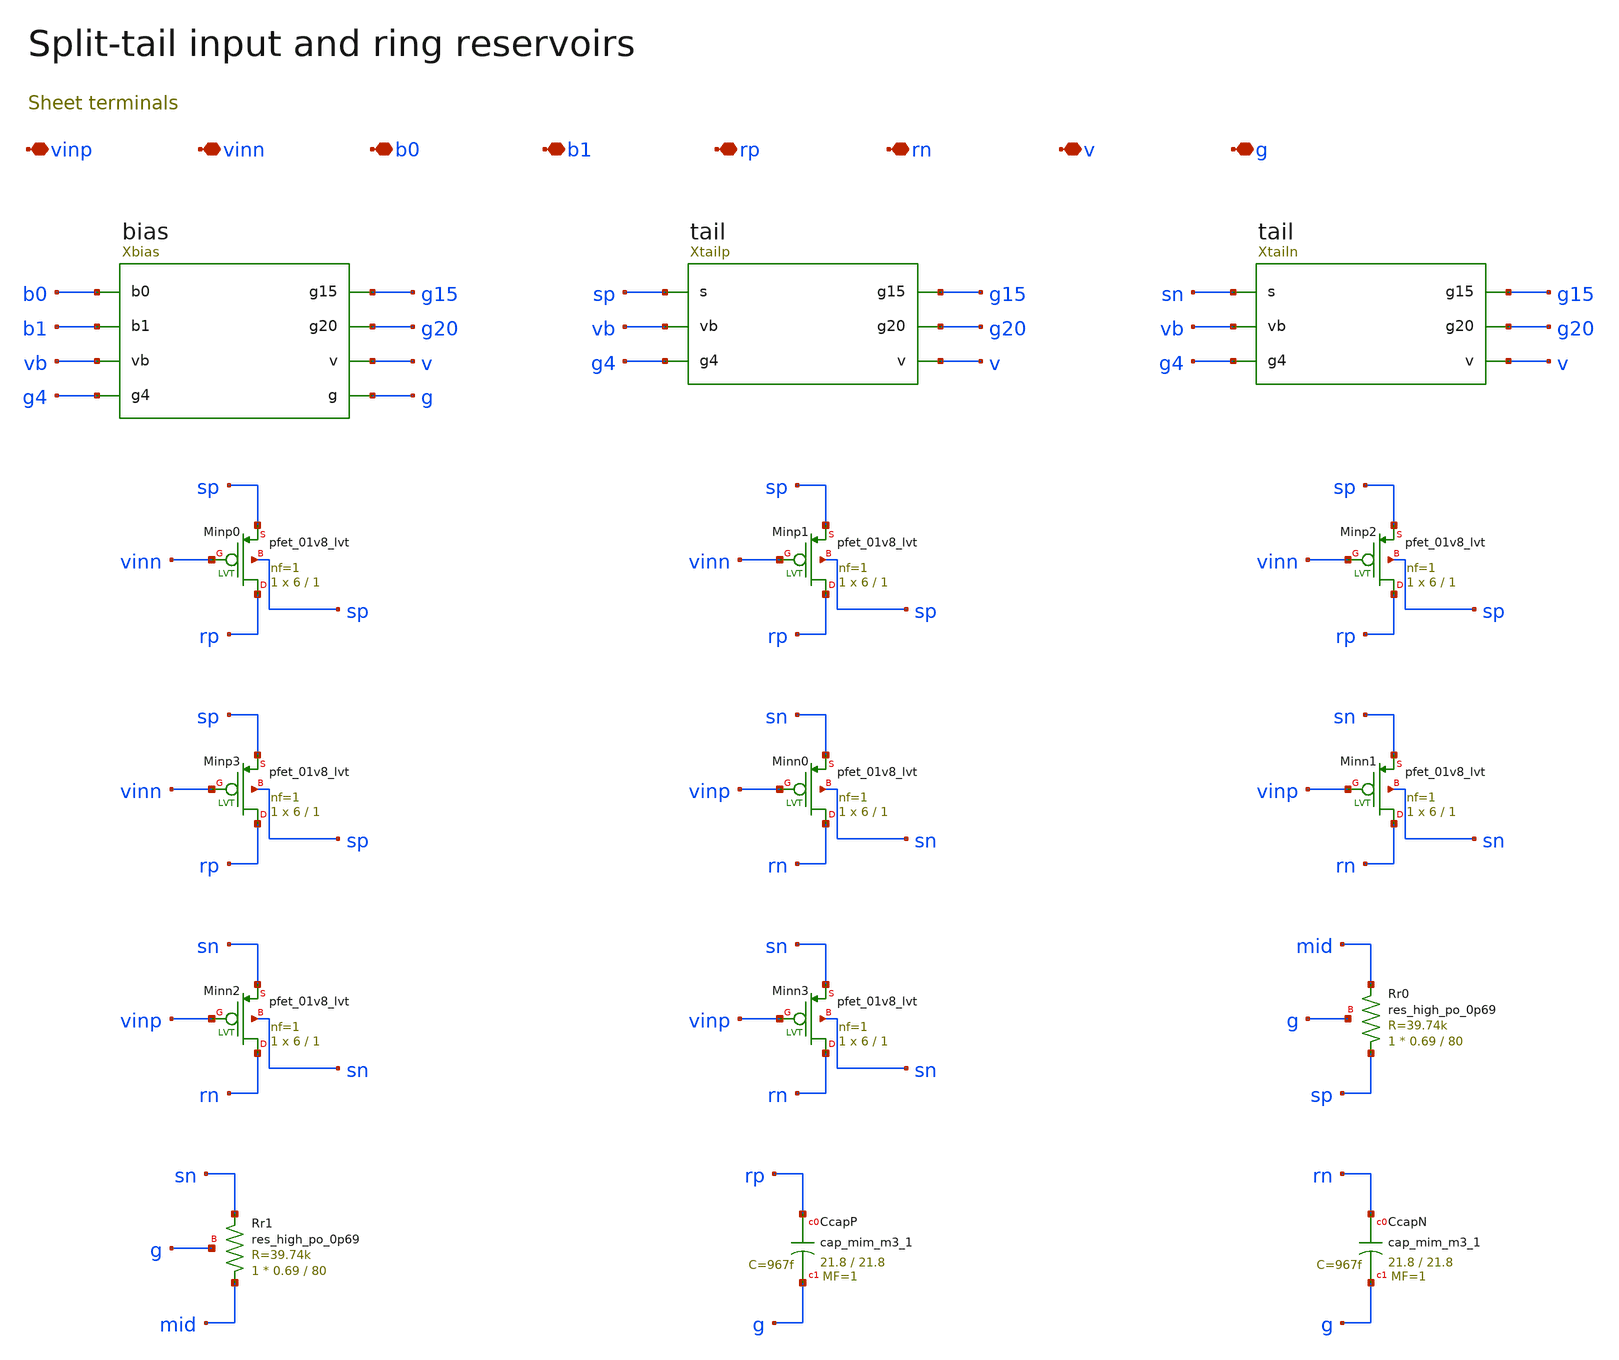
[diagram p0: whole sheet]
** sch_path: review/xschem/front.sch
**.subckt front vinp vinn b0 b1 rp rn v g
*.iopin vinp
*.iopin vinn
*.iopin b0
*.iopin b1
*.iopin rp
*.iopin rn
*.iopin v
*.iopin g
Xbias b0 b1 vb g4 g15 g20 v g bias
Xtailp sp vb g4 g15 g20 v tail
Xtailn sn vb g4 g15 g20 v tail
XMinp0 rp vinn sp sp sky130_fd_pr__pfet_01v8_lvt L=1 W=6 nf=1 ad='int((1 + 1)/2) * 6 / 1 * 0.29' as='int((1 + 2)/2) * 6 / 1 * 0.29'
+ pd='2*int((1 + 1)/2) * (6 / 1 + 0.29)' ps='2*int((1 + 2)/2) * (6 / 1 + 0.29)' nrd='0.29 / 6 ' nrs='0.29 / 6 '
+ sa=0 sb=0 sd=0 mult=1 m=1
XMinp1 rp vinn sp sp sky130_fd_pr__pfet_01v8_lvt L=1 W=6 nf=1 ad='int((1 + 1)/2) * 6 / 1 * 0.29' as='int((1 + 2)/2) * 6 / 1 * 0.29'
+ pd='2*int((1 + 1)/2) * (6 / 1 + 0.29)' ps='2*int((1 + 2)/2) * (6 / 1 + 0.29)' nrd='0.29 / 6 ' nrs='0.29 / 6 '
+ sa=0 sb=0 sd=0 mult=1 m=1
XMinp2 rp vinn sp sp sky130_fd_pr__pfet_01v8_lvt L=1 W=6 nf=1 ad='int((1 + 1)/2) * 6 / 1 * 0.29' as='int((1 + 2)/2) * 6 / 1 * 0.29'
+ pd='2*int((1 + 1)/2) * (6 / 1 + 0.29)' ps='2*int((1 + 2)/2) * (6 / 1 + 0.29)' nrd='0.29 / 6 ' nrs='0.29 / 6 '
+ sa=0 sb=0 sd=0 mult=1 m=1
XMinp3 rp vinn sp sp sky130_fd_pr__pfet_01v8_lvt L=1 W=6 nf=1 ad='int((1 + 1)/2) * 6 / 1 * 0.29' as='int((1 + 2)/2) * 6 / 1 * 0.29'
+ pd='2*int((1 + 1)/2) * (6 / 1 + 0.29)' ps='2*int((1 + 2)/2) * (6 / 1 + 0.29)' nrd='0.29 / 6 ' nrs='0.29 / 6 '
+ sa=0 sb=0 sd=0 mult=1 m=1
XMinn0 rn vinp sn sn sky130_fd_pr__pfet_01v8_lvt L=1 W=6 nf=1 ad='int((1 + 1)/2) * 6 / 1 * 0.29' as='int((1 + 2)/2) * 6 / 1 * 0.29'
+ pd='2*int((1 + 1)/2) * (6 / 1 + 0.29)' ps='2*int((1 + 2)/2) * (6 / 1 + 0.29)' nrd='0.29 / 6 ' nrs='0.29 / 6 '
+ sa=0 sb=0 sd=0 mult=1 m=1
XMinn1 rn vinp sn sn sky130_fd_pr__pfet_01v8_lvt L=1 W=6 nf=1 ad='int((1 + 1)/2) * 6 / 1 * 0.29' as='int((1 + 2)/2) * 6 / 1 * 0.29'
+ pd='2*int((1 + 1)/2) * (6 / 1 + 0.29)' ps='2*int((1 + 2)/2) * (6 / 1 + 0.29)' nrd='0.29 / 6 ' nrs='0.29 / 6 '
+ sa=0 sb=0 sd=0 mult=1 m=1
XMinn2 rn vinp sn sn sky130_fd_pr__pfet_01v8_lvt L=1 W=6 nf=1 ad='int((1 + 1)/2) * 6 / 1 * 0.29' as='int((1 + 2)/2) * 6 / 1 * 0.29'
+ pd='2*int((1 + 1)/2) * (6 / 1 + 0.29)' ps='2*int((1 + 2)/2) * (6 / 1 + 0.29)' nrd='0.29 / 6 ' nrs='0.29 / 6 '
+ sa=0 sb=0 sd=0 mult=1 m=1
XMinn3 rn vinp sn sn sky130_fd_pr__pfet_01v8_lvt L=1 W=6 nf=1 ad='int((1 + 1)/2) * 6 / 1 * 0.29' as='int((1 + 2)/2) * 6 / 1 * 0.29'
+ pd='2*int((1 + 1)/2) * (6 / 1 + 0.29)' ps='2*int((1 + 2)/2) * (6 / 1 + 0.29)' nrd='0.29 / 6 ' nrs='0.29 / 6 '
+ sa=0 sb=0 sd=0 mult=1 m=1
XRr0 sp mid g sky130_fd_pr__res_high_po_0p69 L=80 mult=1 m=1
XRr1 mid sn g sky130_fd_pr__res_high_po_0p69 L=80 mult=1 m=1
XCcapP rp g sky130_fd_pr__cap_mim_m3_1 W=21.8 L=21.8 MF=1 m=1
XCcapN rn g sky130_fd_pr__cap_mim_m3_1 W=21.8 L=21.8 MF=1 m=1
**.ends

* expanding   symbol:  bias.sym # of pins=8
** sym_path: review/xschem/bias.sym
** sch_path: review/xschem/bias.sch
.subckt bias b0 b1 vb g4 g15 g20 v g
*.iopin b0
*.iopin b1
*.iopin vb
*.iopin g4
*.iopin g15
*.iopin g20
*.iopin v
*.iopin g
Xreference vb v g beta_ref
XMi0p nb0 b0 v v sky130_fd_pr__pfet_01v8 L=.15 W=.84 nf=1 ad='int((nf+1)/2) * W/nf * 0.29' as='int((nf+2)/2) * W/nf * 0.29'
+ pd='2*int((nf+1)/2) * (W/nf + 0.29)' ps='2*int((nf+2)/2) * (W/nf + 0.29)' nrd='0.29 / W' nrs='0.29 / W'
+ sa=0 sb=0 sd=0 mult=1 m=1
XMi0n nb0 b0 g g sky130_fd_pr__nfet_01v8 L=.15 W=.42 nf=1 ad='int((1 + 1)/2) * .42 / 1 * 0.29' as='int((1 + 2)/2) * .42 / 1 * 0.29'
+ pd='2*int((1 + 1)/2) * (.42 / 1 + 0.29)' ps='2*int((1 + 2)/2) * (.42 / 1 + 0.29)' nrd='0.29 / .42 ' nrs='0.29 / .42 '
+ sa=0 sb=0 sd=0 mult=1 m=1
XMi1p nb1 b1 v v sky130_fd_pr__pfet_01v8 L=.15 W=.84 nf=1 ad='int((nf+1)/2) * W/nf * 0.29' as='int((nf+2)/2) * W/nf * 0.29'
+ pd='2*int((nf+1)/2) * (W/nf + 0.29)' ps='2*int((nf+2)/2) * (W/nf + 0.29)' nrd='0.29 / W' nrs='0.29 / W'
+ sa=0 sb=0 sd=0 mult=1 m=1
XMi1n nb1 b1 g g sky130_fd_pr__nfet_01v8 L=.15 W=.42 nf=1 ad='int((1 + 1)/2) * .42 / 1 * 0.29' as='int((1 + 2)/2) * .42 / 1 * 0.29'
+ pd='2*int((1 + 1)/2) * (.42 / 1 + 0.29)' ps='2*int((1 + 2)/2) * (.42 / 1 + 0.29)' nrd='0.29 / .42 ' nrs='0.29 / .42 '
+ sa=0 sb=0 sd=0 mult=1 m=1
Xonlylow nb0 b1 off4 v g nor2
XMi4p en4 off4 v v sky130_fd_pr__pfet_01v8 L=.15 W=.84 nf=1 ad='int((nf+1)/2) * W/nf * 0.29' as='int((nf+2)/2) * W/nf * 0.29'
+ pd='2*int((nf+1)/2) * (W/nf + 0.29)' ps='2*int((nf+2)/2) * (W/nf + 0.29)' nrd='0.29 / W' nrs='0.29 / W'
+ sa=0 sb=0 sd=0 mult=1 m=1
XMi4n en4 off4 g g sky130_fd_pr__nfet_01v8 L=.15 W=.42 nf=1 ad='int((1 + 1)/2) * .42 / 1 * 0.29' as='int((1 + 2)/2) * .42 / 1 * 0.29'
+ pd='2*int((1 + 1)/2) * (.42 / 1 + 0.29)' ps='2*int((1 + 2)/2) * (.42 / 1 + 0.29)' nrd='0.29 / .42 ' nrs='0.29 / .42 '
+ sa=0 sb=0 sd=0 mult=1 m=1
Xboth nb0 nb1 en20 v g nor2
Xzero b0 b1 zero v g nor2
Xdiff zero en20 off15 v g nor2
XMi15p en15 off15 v v sky130_fd_pr__pfet_01v8 L=.15 W=.84 nf=1 ad='int((nf+1)/2) * W/nf * 0.29' as='int((nf+2)/2) * W/nf * 0.29'
+ pd='2*int((nf+1)/2) * (W/nf + 0.29)' ps='2*int((nf+2)/2) * (W/nf + 0.29)' nrd='0.29 / W' nrs='0.29 / W'
+ sa=0 sb=0 sd=0 mult=1 m=1
XMi15n en15 off15 g g sky130_fd_pr__nfet_01v8 L=.15 W=.42 nf=1 ad='int((1 + 1)/2) * .42 / 1 * 0.29' as='int((1 + 2)/2) * .42 / 1 * 0.29'
+ pd='2*int((1 + 1)/2) * (.42 / 1 + 0.29)' ps='2*int((1 + 2)/2) * (.42 / 1 + 0.29)' nrd='0.29 / .42 ' nrs='0.29 / .42 '
+ sa=0 sb=0 sd=0 mult=1 m=1
XMi20p off20 en20 v v sky130_fd_pr__pfet_01v8 L=.15 W=.84 nf=1 ad='int((nf+1)/2) * W/nf * 0.29' as='int((nf+2)/2) * W/nf * 0.29'
+ pd='2*int((nf+1)/2) * (W/nf + 0.29)' ps='2*int((nf+2)/2) * (W/nf + 0.29)' nrd='0.29 / W' nrs='0.29 / W'
+ sa=0 sb=0 sd=0 mult=1 m=1
XMi20n off20 en20 g g sky130_fd_pr__nfet_01v8 L=.15 W=.42 nf=1 ad='int((1 + 1)/2) * .42 / 1 * 0.29' as='int((1 + 2)/2) * .42 / 1 * 0.29'
+ pd='2*int((1 + 1)/2) * (.42 / 1 + 0.29)' ps='2*int((1 + 2)/2) * (.42 / 1 + 0.29)' nrd='0.29 / .42 ' nrs='0.29 / .42 '
+ sa=0 sb=0 sd=0 mult=1 m=1
Xsw4 en4 off4 vb g4 v g tailgate
Xsw15 en15 off15 vb g15 v g tailgate
Xsw20 en20 off20 vb g20 v g tailgate
.ends


* expanding   symbol:  tail.sym # of pins=6
** sym_path: review/xschem/tail.sym
** sch_path: review/xschem/tail.sch
.subckt tail s vb g4 g15 g20 v
*.iopin s
*.iopin vb
*.iopin g4
*.iopin g15
*.iopin g20
*.iopin v
XMone s vb v v sky130_fd_pr__pfet_01v8 L=2 W=1 nf=1 ad='int((nf+1)/2) * W/nf * 0.29' as='int((nf+2)/2) * W/nf * 0.29'
+ pd='2*int((nf+1)/2) * (W/nf + 0.29)' ps='2*int((nf+2)/2) * (W/nf + 0.29)' nrd='0.29 / W' nrs='0.29 / W'
+ sa=0 sb=0 sd=0 mult=1 m=1
Xunits4 s g4 v units4
Xunits15 s g15 v units15
Xunits20 s g20 v units20
.ends


* expanding   symbol:  beta_ref.sym # of pins=3
** sym_path: review/xschem/beta_ref.sym
** sch_path: review/xschem/beta_ref.sch
.subckt beta_ref vb v g
*.iopin vb
*.iopin v
*.iopin g
XMp0 vb vb v v sky130_fd_pr__pfet_01v8 L=2 W=2 nf=1 ad='int((nf+1)/2) * W/nf * 0.29' as='int((nf+2)/2) * W/nf * 0.29'
+ pd='2*int((nf+1)/2) * (W/nf + 0.29)' ps='2*int((nf+2)/2) * (W/nf + 0.29)' nrd='0.29 / W' nrs='0.29 / W'
+ sa=0 sb=0 sd=0 mult=1 m=1
XMn0 vn vn g g sky130_fd_pr__nfet_01v8 L=2 W=2 nf=1 ad='int((1 + 1)/2) * 2 / 1 * 0.29' as='int((1 + 2)/2) * 2 / 1 * 0.29'
+ pd='2*int((1 + 1)/2) * (2 / 1 + 0.29)' ps='2*int((1 + 2)/2) * (2 / 1 + 0.29)' nrd='0.29 / 2 ' nrs='0.29 / 2 '
+ sa=0 sb=0 sd=0 mult=1 m=1
XMp1 vn vb v v sky130_fd_pr__pfet_01v8 L=2 W=2 nf=1 ad='int((nf+1)/2) * W/nf * 0.29' as='int((nf+2)/2) * W/nf * 0.29'
+ pd='2*int((nf+1)/2) * (W/nf + 0.29)' ps='2*int((nf+2)/2) * (W/nf + 0.29)' nrd='0.29 / W' nrs='0.29 / W'
+ sa=0 sb=0 sd=0 mult=1 m=1
XMn1 vb vn rs g sky130_fd_pr__nfet_01v8 L=2 W=8 nf=1 ad='int((1 + 1)/2) * 8 / 1 * 0.29' as='int((1 + 2)/2) * 8 / 1 * 0.29'
+ pd='2*int((1 + 1)/2) * (8 / 1 + 0.29)' ps='2*int((1 + 2)/2) * (8 / 1 + 0.29)' nrd='0.29 / 8 ' nrs='0.29 / 8 '
+ sa=0 sb=0 sd=0 mult=1 m=1
XRref0 rs refmid g sky130_fd_pr__res_high_po_0p69 L=97.1 mult=1 m=1
XRref1 refmid g g sky130_fd_pr__res_high_po_0p69 L=97.1 mult=1 m=1
XMweak kick g v v sky130_fd_pr__pfet_01v8 L=12 W=.42 nf=1 ad='int((nf+1)/2) * W/nf * 0.29' as='int((nf+2)/2) * W/nf * 0.29'
+ pd='2*int((nf+1)/2) * (W/nf + 0.29)' ps='2*int((nf+2)/2) * (W/nf + 0.29)' nrd='0.29 / W' nrs='0.29 / W'
+ sa=0 sb=0 sd=0 mult=1 m=1
XMsense kick vn g g sky130_fd_pr__nfet_01v8_lvt L=.15 W=5 nf=1 ad='int((1 + 1)/2) * 5 / 1 * 0.29' as='int((1 + 2)/2) * 5 / 1 * 0.29'
+ pd='2*int((1 + 1)/2) * (5 / 1 + 0.29)' ps='2*int((1 + 2)/2) * (5 / 1 + 0.29)' nrd='0.29 / 5 ' nrs='0.29 / 5 '
+ sa=0 sb=0 sd=0 mult=1 m=1
XMkick vb kick g g sky130_fd_pr__nfet_01v8 L=1 W=.5 nf=1 ad='int((1 + 1)/2) * .5 / 1 * 0.29' as='int((1 + 2)/2) * .5 / 1 * 0.29'
+ pd='2*int((1 + 1)/2) * (.5 / 1 + 0.29)' ps='2*int((1 + 2)/2) * (.5 / 1 + 0.29)' nrd='0.29 / .5 ' nrs='0.29 / .5 '
+ sa=0 sb=0 sd=0 mult=1 m=1
.ends


* expanding   symbol:  nor2.sym # of pins=5
** sym_path: review/xschem/nor2.sym
** sch_path: review/xschem/nor2.sch
.subckt nor2 a b y v g
*.iopin a
*.iopin b
*.iopin y
*.iopin v
*.iopin g
XMp0 mid a v v sky130_fd_pr__pfet_01v8 L=.15 W=.84 nf=1 ad='int((nf+1)/2) * W/nf * 0.29' as='int((nf+2)/2) * W/nf * 0.29'
+ pd='2*int((nf+1)/2) * (W/nf + 0.29)' ps='2*int((nf+2)/2) * (W/nf + 0.29)' nrd='0.29 / W' nrs='0.29 / W'
+ sa=0 sb=0 sd=0 mult=1 m=1
XMp1 y b mid v sky130_fd_pr__pfet_01v8 L=.15 W=.84 nf=1 ad='int((nf+1)/2) * W/nf * 0.29' as='int((nf+2)/2) * W/nf * 0.29'
+ pd='2*int((nf+1)/2) * (W/nf + 0.29)' ps='2*int((nf+2)/2) * (W/nf + 0.29)' nrd='0.29 / W' nrs='0.29 / W'
+ sa=0 sb=0 sd=0 mult=1 m=1
XMn0 y a g g sky130_fd_pr__nfet_01v8 L=.15 W=.42 nf=1 ad='int((1 + 1)/2) * .42 / 1 * 0.29' as='int((1 + 2)/2) * .42 / 1 * 0.29'
+ pd='2*int((1 + 1)/2) * (.42 / 1 + 0.29)' ps='2*int((1 + 2)/2) * (.42 / 1 + 0.29)' nrd='0.29 / .42 ' nrs='0.29 / .42 '
+ sa=0 sb=0 sd=0 mult=1 m=1
XMn1 y b g g sky130_fd_pr__nfet_01v8 L=.15 W=.42 nf=1 ad='int((1 + 1)/2) * .42 / 1 * 0.29' as='int((1 + 2)/2) * .42 / 1 * 0.29'
+ pd='2*int((1 + 1)/2) * (.42 / 1 + 0.29)' ps='2*int((1 + 2)/2) * (.42 / 1 + 0.29)' nrd='0.29 / .42 ' nrs='0.29 / .42 '
+ sa=0 sb=0 sd=0 mult=1 m=1
.ends


* expanding   symbol:  tailgate.sym # of pins=6
** sym_path: review/xschem/tailgate.sym
** sch_path: review/xschem/tailgate.sch
.subckt tailgate en enb vb out v g
*.iopin en
*.iopin enb
*.iopin vb
*.iopin out
*.iopin v
*.iopin g
XMonp out enb vb v sky130_fd_pr__pfet_01v8 L=.15 W=.84 nf=1 ad='int((nf+1)/2) * W/nf * 0.29' as='int((nf+2)/2) * W/nf * 0.29'
+ pd='2*int((nf+1)/2) * (W/nf + 0.29)' ps='2*int((nf+2)/2) * (W/nf + 0.29)' nrd='0.29 / W' nrs='0.29 / W'
+ sa=0 sb=0 sd=0 mult=1 m=1
XMonn out en vb g sky130_fd_pr__nfet_01v8 L=.15 W=.42 nf=1 ad='int((1 + 1)/2) * .42 / 1 * 0.29' as='int((1 + 2)/2) * .42 / 1 * 0.29'
+ pd='2*int((1 + 1)/2) * (.42 / 1 + 0.29)' ps='2*int((1 + 2)/2) * (.42 / 1 + 0.29)' nrd='0.29 / .42 ' nrs='0.29 / .42 '
+ sa=0 sb=0 sd=0 mult=1 m=1
XMoff out en v v sky130_fd_pr__pfet_01v8 L=.15 W=.84 nf=1 ad='int((nf+1)/2) * W/nf * 0.29' as='int((nf+2)/2) * W/nf * 0.29'
+ pd='2*int((nf+1)/2) * (W/nf + 0.29)' ps='2*int((nf+2)/2) * (W/nf + 0.29)' nrd='0.29 / W' nrs='0.29 / W'
+ sa=0 sb=0 sd=0 mult=1 m=1
.ends


* expanding   symbol:  units4.sym # of pins=3
** sym_path: review/xschem/units4.sym
** sch_path: review/xschem/units4.sch
.subckt units4 s control v
*.iopin s
*.iopin control
*.iopin v
XMg4_1 s control v v sky130_fd_pr__pfet_01v8 L=2 W=1 nf=1 ad='int((nf+1)/2) * W/nf * 0.29' as='int((nf+2)/2) * W/nf * 0.29'
+ pd='2*int((nf+1)/2) * (W/nf + 0.29)' ps='2*int((nf+2)/2) * (W/nf + 0.29)' nrd='0.29 / W' nrs='0.29 / W'
+ sa=0 sb=0 sd=0 mult=1 m=1
XMg4_2 s control v v sky130_fd_pr__pfet_01v8 L=2 W=1 nf=1 ad='int((nf+1)/2) * W/nf * 0.29' as='int((nf+2)/2) * W/nf * 0.29'
+ pd='2*int((nf+1)/2) * (W/nf + 0.29)' ps='2*int((nf+2)/2) * (W/nf + 0.29)' nrd='0.29 / W' nrs='0.29 / W'
+ sa=0 sb=0 sd=0 mult=1 m=1
XMg4_3 s control v v sky130_fd_pr__pfet_01v8 L=2 W=1 nf=1 ad='int((nf+1)/2) * W/nf * 0.29' as='int((nf+2)/2) * W/nf * 0.29'
+ pd='2*int((nf+1)/2) * (W/nf + 0.29)' ps='2*int((nf+2)/2) * (W/nf + 0.29)' nrd='0.29 / W' nrs='0.29 / W'
+ sa=0 sb=0 sd=0 mult=1 m=1
XMg4_4 s control v v sky130_fd_pr__pfet_01v8 L=2 W=1 nf=1 ad='int((nf+1)/2) * W/nf * 0.29' as='int((nf+2)/2) * W/nf * 0.29'
+ pd='2*int((nf+1)/2) * (W/nf + 0.29)' ps='2*int((nf+2)/2) * (W/nf + 0.29)' nrd='0.29 / W' nrs='0.29 / W'
+ sa=0 sb=0 sd=0 mult=1 m=1
.ends


* expanding   symbol:  units15.sym # of pins=3
** sym_path: review/xschem/units15.sym
** sch_path: review/xschem/units15.sch
.subckt units15 s control v
*.iopin s
*.iopin control
*.iopin v
XMg15_1 s control v v sky130_fd_pr__pfet_01v8 L=2 W=1 nf=1 ad='int((nf+1)/2) * W/nf * 0.29' as='int((nf+2)/2) * W/nf * 0.29'
+ pd='2*int((nf+1)/2) * (W/nf + 0.29)' ps='2*int((nf+2)/2) * (W/nf + 0.29)' nrd='0.29 / W' nrs='0.29 / W'
+ sa=0 sb=0 sd=0 mult=1 m=1
XMg15_2 s control v v sky130_fd_pr__pfet_01v8 L=2 W=1 nf=1 ad='int((nf+1)/2) * W/nf * 0.29' as='int((nf+2)/2) * W/nf * 0.29'
+ pd='2*int((nf+1)/2) * (W/nf + 0.29)' ps='2*int((nf+2)/2) * (W/nf + 0.29)' nrd='0.29 / W' nrs='0.29 / W'
+ sa=0 sb=0 sd=0 mult=1 m=1
XMg15_3 s control v v sky130_fd_pr__pfet_01v8 L=2 W=1 nf=1 ad='int((nf+1)/2) * W/nf * 0.29' as='int((nf+2)/2) * W/nf * 0.29'
+ pd='2*int((nf+1)/2) * (W/nf + 0.29)' ps='2*int((nf+2)/2) * (W/nf + 0.29)' nrd='0.29 / W' nrs='0.29 / W'
+ sa=0 sb=0 sd=0 mult=1 m=1
XMg15_4 s control v v sky130_fd_pr__pfet_01v8 L=2 W=1 nf=1 ad='int((nf+1)/2) * W/nf * 0.29' as='int((nf+2)/2) * W/nf * 0.29'
+ pd='2*int((nf+1)/2) * (W/nf + 0.29)' ps='2*int((nf+2)/2) * (W/nf + 0.29)' nrd='0.29 / W' nrs='0.29 / W'
+ sa=0 sb=0 sd=0 mult=1 m=1
XMg15_5 s control v v sky130_fd_pr__pfet_01v8 L=2 W=1 nf=1 ad='int((nf+1)/2) * W/nf * 0.29' as='int((nf+2)/2) * W/nf * 0.29'
+ pd='2*int((nf+1)/2) * (W/nf + 0.29)' ps='2*int((nf+2)/2) * (W/nf + 0.29)' nrd='0.29 / W' nrs='0.29 / W'
+ sa=0 sb=0 sd=0 mult=1 m=1
XMg15_6 s control v v sky130_fd_pr__pfet_01v8 L=2 W=1 nf=1 ad='int((nf+1)/2) * W/nf * 0.29' as='int((nf+2)/2) * W/nf * 0.29'
+ pd='2*int((nf+1)/2) * (W/nf + 0.29)' ps='2*int((nf+2)/2) * (W/nf + 0.29)' nrd='0.29 / W' nrs='0.29 / W'
+ sa=0 sb=0 sd=0 mult=1 m=1
XMg15_7 s control v v sky130_fd_pr__pfet_01v8 L=2 W=1 nf=1 ad='int((nf+1)/2) * W/nf * 0.29' as='int((nf+2)/2) * W/nf * 0.29'
+ pd='2*int((nf+1)/2) * (W/nf + 0.29)' ps='2*int((nf+2)/2) * (W/nf + 0.29)' nrd='0.29 / W' nrs='0.29 / W'
+ sa=0 sb=0 sd=0 mult=1 m=1
XMg15_8 s control v v sky130_fd_pr__pfet_01v8 L=2 W=1 nf=1 ad='int((nf+1)/2) * W/nf * 0.29' as='int((nf+2)/2) * W/nf * 0.29'
+ pd='2*int((nf+1)/2) * (W/nf + 0.29)' ps='2*int((nf+2)/2) * (W/nf + 0.29)' nrd='0.29 / W' nrs='0.29 / W'
+ sa=0 sb=0 sd=0 mult=1 m=1
XMg15_9 s control v v sky130_fd_pr__pfet_01v8 L=2 W=1 nf=1 ad='int((nf+1)/2) * W/nf * 0.29' as='int((nf+2)/2) * W/nf * 0.29'
+ pd='2*int((nf+1)/2) * (W/nf + 0.29)' ps='2*int((nf+2)/2) * (W/nf + 0.29)' nrd='0.29 / W' nrs='0.29 / W'
+ sa=0 sb=0 sd=0 mult=1 m=1
XMg15_10 s control v v sky130_fd_pr__pfet_01v8 L=2 W=1 nf=1 ad='int((nf+1)/2) * W/nf * 0.29' as='int((nf+2)/2) * W/nf * 0.29'
+ pd='2*int((nf+1)/2) * (W/nf + 0.29)' ps='2*int((nf+2)/2) * (W/nf + 0.29)' nrd='0.29 / W' nrs='0.29 / W'
+ sa=0 sb=0 sd=0 mult=1 m=1
XMg15_11 s control v v sky130_fd_pr__pfet_01v8 L=2 W=1 nf=1 ad='int((nf+1)/2) * W/nf * 0.29' as='int((nf+2)/2) * W/nf * 0.29'
+ pd='2*int((nf+1)/2) * (W/nf + 0.29)' ps='2*int((nf+2)/2) * (W/nf + 0.29)' nrd='0.29 / W' nrs='0.29 / W'
+ sa=0 sb=0 sd=0 mult=1 m=1
XMg15_12 s control v v sky130_fd_pr__pfet_01v8 L=2 W=1 nf=1 ad='int((nf+1)/2) * W/nf * 0.29' as='int((nf+2)/2) * W/nf * 0.29'
+ pd='2*int((nf+1)/2) * (W/nf + 0.29)' ps='2*int((nf+2)/2) * (W/nf + 0.29)' nrd='0.29 / W' nrs='0.29 / W'
+ sa=0 sb=0 sd=0 mult=1 m=1
XMg15_13 s control v v sky130_fd_pr__pfet_01v8 L=2 W=1 nf=1 ad='int((nf+1)/2) * W/nf * 0.29' as='int((nf+2)/2) * W/nf * 0.29'
+ pd='2*int((nf+1)/2) * (W/nf + 0.29)' ps='2*int((nf+2)/2) * (W/nf + 0.29)' nrd='0.29 / W' nrs='0.29 / W'
+ sa=0 sb=0 sd=0 mult=1 m=1
XMg15_14 s control v v sky130_fd_pr__pfet_01v8 L=2 W=1 nf=1 ad='int((nf+1)/2) * W/nf * 0.29' as='int((nf+2)/2) * W/nf * 0.29'
+ pd='2*int((nf+1)/2) * (W/nf + 0.29)' ps='2*int((nf+2)/2) * (W/nf + 0.29)' nrd='0.29 / W' nrs='0.29 / W'
+ sa=0 sb=0 sd=0 mult=1 m=1
XMg15_15 s control v v sky130_fd_pr__pfet_01v8 L=2 W=1 nf=1 ad='int((nf+1)/2) * W/nf * 0.29' as='int((nf+2)/2) * W/nf * 0.29'
+ pd='2*int((nf+1)/2) * (W/nf + 0.29)' ps='2*int((nf+2)/2) * (W/nf + 0.29)' nrd='0.29 / W' nrs='0.29 / W'
+ sa=0 sb=0 sd=0 mult=1 m=1
.ends


* expanding   symbol:  units20.sym # of pins=3
** sym_path: review/xschem/units20.sym
** sch_path: review/xschem/units20.sch
.subckt units20 s control v
*.iopin s
*.iopin control
*.iopin v
XMg20_1 s control v v sky130_fd_pr__pfet_01v8 L=2 W=1 nf=1 ad='int((nf+1)/2) * W/nf * 0.29' as='int((nf+2)/2) * W/nf * 0.29'
+ pd='2*int((nf+1)/2) * (W/nf + 0.29)' ps='2*int((nf+2)/2) * (W/nf + 0.29)' nrd='0.29 / W' nrs='0.29 / W'
+ sa=0 sb=0 sd=0 mult=1 m=1
XMg20_2 s control v v sky130_fd_pr__pfet_01v8 L=2 W=1 nf=1 ad='int((nf+1)/2) * W/nf * 0.29' as='int((nf+2)/2) * W/nf * 0.29'
+ pd='2*int((nf+1)/2) * (W/nf + 0.29)' ps='2*int((nf+2)/2) * (W/nf + 0.29)' nrd='0.29 / W' nrs='0.29 / W'
+ sa=0 sb=0 sd=0 mult=1 m=1
XMg20_3 s control v v sky130_fd_pr__pfet_01v8 L=2 W=1 nf=1 ad='int((nf+1)/2) * W/nf * 0.29' as='int((nf+2)/2) * W/nf * 0.29'
+ pd='2*int((nf+1)/2) * (W/nf + 0.29)' ps='2*int((nf+2)/2) * (W/nf + 0.29)' nrd='0.29 / W' nrs='0.29 / W'
+ sa=0 sb=0 sd=0 mult=1 m=1
XMg20_4 s control v v sky130_fd_pr__pfet_01v8 L=2 W=1 nf=1 ad='int((nf+1)/2) * W/nf * 0.29' as='int((nf+2)/2) * W/nf * 0.29'
+ pd='2*int((nf+1)/2) * (W/nf + 0.29)' ps='2*int((nf+2)/2) * (W/nf + 0.29)' nrd='0.29 / W' nrs='0.29 / W'
+ sa=0 sb=0 sd=0 mult=1 m=1
XMg20_5 s control v v sky130_fd_pr__pfet_01v8 L=2 W=1 nf=1 ad='int((nf+1)/2) * W/nf * 0.29' as='int((nf+2)/2) * W/nf * 0.29'
+ pd='2*int((nf+1)/2) * (W/nf + 0.29)' ps='2*int((nf+2)/2) * (W/nf + 0.29)' nrd='0.29 / W' nrs='0.29 / W'
+ sa=0 sb=0 sd=0 mult=1 m=1
XMg20_6 s control v v sky130_fd_pr__pfet_01v8 L=2 W=1 nf=1 ad='int((nf+1)/2) * W/nf * 0.29' as='int((nf+2)/2) * W/nf * 0.29'
+ pd='2*int((nf+1)/2) * (W/nf + 0.29)' ps='2*int((nf+2)/2) * (W/nf + 0.29)' nrd='0.29 / W' nrs='0.29 / W'
+ sa=0 sb=0 sd=0 mult=1 m=1
XMg20_7 s control v v sky130_fd_pr__pfet_01v8 L=2 W=1 nf=1 ad='int((nf+1)/2) * W/nf * 0.29' as='int((nf+2)/2) * W/nf * 0.29'
+ pd='2*int((nf+1)/2) * (W/nf + 0.29)' ps='2*int((nf+2)/2) * (W/nf + 0.29)' nrd='0.29 / W' nrs='0.29 / W'
+ sa=0 sb=0 sd=0 mult=1 m=1
XMg20_8 s control v v sky130_fd_pr__pfet_01v8 L=2 W=1 nf=1 ad='int((nf+1)/2) * W/nf * 0.29' as='int((nf+2)/2) * W/nf * 0.29'
+ pd='2*int((nf+1)/2) * (W/nf + 0.29)' ps='2*int((nf+2)/2) * (W/nf + 0.29)' nrd='0.29 / W' nrs='0.29 / W'
+ sa=0 sb=0 sd=0 mult=1 m=1
XMg20_9 s control v v sky130_fd_pr__pfet_01v8 L=2 W=1 nf=1 ad='int((nf+1)/2) * W/nf * 0.29' as='int((nf+2)/2) * W/nf * 0.29'
+ pd='2*int((nf+1)/2) * (W/nf + 0.29)' ps='2*int((nf+2)/2) * (W/nf + 0.29)' nrd='0.29 / W' nrs='0.29 / W'
+ sa=0 sb=0 sd=0 mult=1 m=1
XMg20_10 s control v v sky130_fd_pr__pfet_01v8 L=2 W=1 nf=1 ad='int((nf+1)/2) * W/nf * 0.29' as='int((nf+2)/2) * W/nf * 0.29'
+ pd='2*int((nf+1)/2) * (W/nf + 0.29)' ps='2*int((nf+2)/2) * (W/nf + 0.29)' nrd='0.29 / W' nrs='0.29 / W'
+ sa=0 sb=0 sd=0 mult=1 m=1
XMg20_11 s control v v sky130_fd_pr__pfet_01v8 L=2 W=1 nf=1 ad='int((nf+1)/2) * W/nf * 0.29' as='int((nf+2)/2) * W/nf * 0.29'
+ pd='2*int((nf+1)/2) * (W/nf + 0.29)' ps='2*int((nf+2)/2) * (W/nf + 0.29)' nrd='0.29 / W' nrs='0.29 / W'
+ sa=0 sb=0 sd=0 mult=1 m=1
XMg20_12 s control v v sky130_fd_pr__pfet_01v8 L=2 W=1 nf=1 ad='int((nf+1)/2) * W/nf * 0.29' as='int((nf+2)/2) * W/nf * 0.29'
+ pd='2*int((nf+1)/2) * (W/nf + 0.29)' ps='2*int((nf+2)/2) * (W/nf + 0.29)' nrd='0.29 / W' nrs='0.29 / W'
+ sa=0 sb=0 sd=0 mult=1 m=1
XMg20_13 s control v v sky130_fd_pr__pfet_01v8 L=2 W=1 nf=1 ad='int((nf+1)/2) * W/nf * 0.29' as='int((nf+2)/2) * W/nf * 0.29'
+ pd='2*int((nf+1)/2) * (W/nf + 0.29)' ps='2*int((nf+2)/2) * (W/nf + 0.29)' nrd='0.29 / W' nrs='0.29 / W'
+ sa=0 sb=0 sd=0 mult=1 m=1
XMg20_14 s control v v sky130_fd_pr__pfet_01v8 L=2 W=1 nf=1 ad='int((nf+1)/2) * W/nf * 0.29' as='int((nf+2)/2) * W/nf * 0.29'
+ pd='2*int((nf+1)/2) * (W/nf + 0.29)' ps='2*int((nf+2)/2) * (W/nf + 0.29)' nrd='0.29 / W' nrs='0.29 / W'
+ sa=0 sb=0 sd=0 mult=1 m=1
XMg20_15 s control v v sky130_fd_pr__pfet_01v8 L=2 W=1 nf=1 ad='int((nf+1)/2) * W/nf * 0.29' as='int((nf+2)/2) * W/nf * 0.29'
+ pd='2*int((nf+1)/2) * (W/nf + 0.29)' ps='2*int((nf+2)/2) * (W/nf + 0.29)' nrd='0.29 / W' nrs='0.29 / W'
+ sa=0 sb=0 sd=0 mult=1 m=1
XMg20_16 s control v v sky130_fd_pr__pfet_01v8 L=2 W=1 nf=1 ad='int((nf+1)/2) * W/nf * 0.29' as='int((nf+2)/2) * W/nf * 0.29'
+ pd='2*int((nf+1)/2) * (W/nf + 0.29)' ps='2*int((nf+2)/2) * (W/nf + 0.29)' nrd='0.29 / W' nrs='0.29 / W'
+ sa=0 sb=0 sd=0 mult=1 m=1
XMg20_17 s control v v sky130_fd_pr__pfet_01v8 L=2 W=1 nf=1 ad='int((nf+1)/2) * W/nf * 0.29' as='int((nf+2)/2) * W/nf * 0.29'
+ pd='2*int((nf+1)/2) * (W/nf + 0.29)' ps='2*int((nf+2)/2) * (W/nf + 0.29)' nrd='0.29 / W' nrs='0.29 / W'
+ sa=0 sb=0 sd=0 mult=1 m=1
XMg20_18 s control v v sky130_fd_pr__pfet_01v8 L=2 W=1 nf=1 ad='int((nf+1)/2) * W/nf * 0.29' as='int((nf+2)/2) * W/nf * 0.29'
+ pd='2*int((nf+1)/2) * (W/nf + 0.29)' ps='2*int((nf+2)/2) * (W/nf + 0.29)' nrd='0.29 / W' nrs='0.29 / W'
+ sa=0 sb=0 sd=0 mult=1 m=1
XMg20_19 s control v v sky130_fd_pr__pfet_01v8 L=2 W=1 nf=1 ad='int((nf+1)/2) * W/nf * 0.29' as='int((nf+2)/2) * W/nf * 0.29'
+ pd='2*int((nf+1)/2) * (W/nf + 0.29)' ps='2*int((nf+2)/2) * (W/nf + 0.29)' nrd='0.29 / W' nrs='0.29 / W'
+ sa=0 sb=0 sd=0 mult=1 m=1
XMg20_20 s control v v sky130_fd_pr__pfet_01v8 L=2 W=1 nf=1 ad='int((nf+1)/2) * W/nf * 0.29' as='int((nf+2)/2) * W/nf * 0.29'
+ pd='2*int((nf+1)/2) * (W/nf + 0.29)' ps='2*int((nf+2)/2) * (W/nf + 0.29)' nrd='0.29 / W' nrs='0.29 / W'
+ sa=0 sb=0 sd=0 mult=1 m=1
.ends

.end
